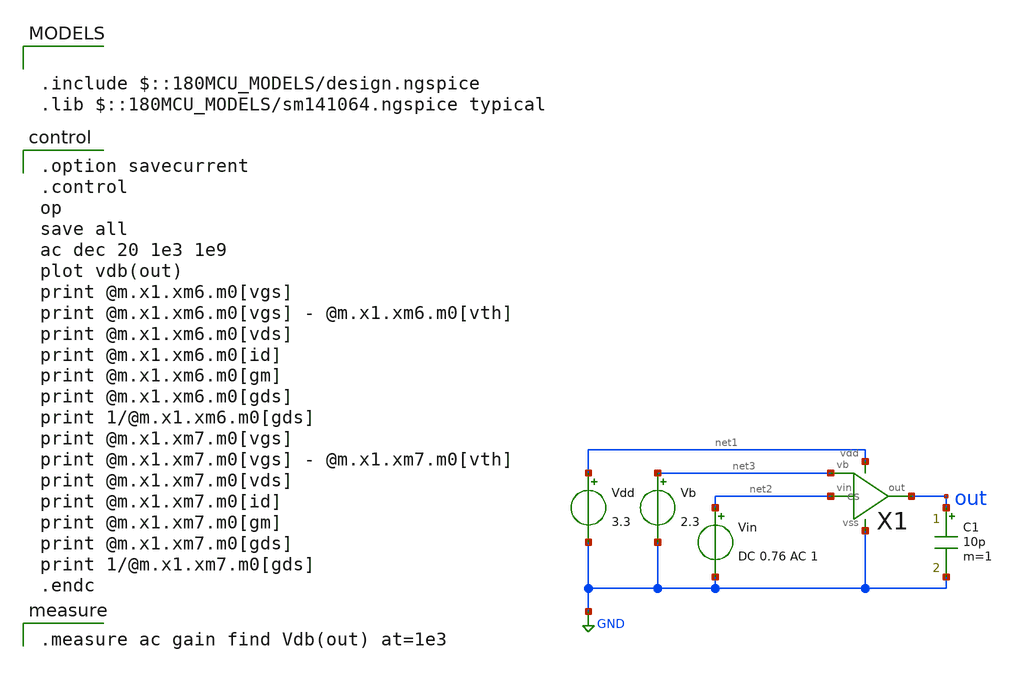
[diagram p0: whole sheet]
** sch_path: opamp/cs_ac.sch
**.subckt cs_ac
Vdd net1 GND 3.3
Vb net3 GND 2.3
Vin net2 GND DC 0.76 AC 1
X1 net2 net3 out net1 GND cs
C1 out GND 10p m=1
**** begin user architecture code

.include $::180MCU_MODELS/design.ngspice
.lib $::180MCU_MODELS/sm141064.ngspice typical


.option savecurrent
.control
op
save all
ac dec 20 1e3 1e9
plot vdb(out)
print @m.x1.xm6.m0[vgs]
print @m.x1.xm6.m0[vgs] - @m.x1.xm6.m0[vth]
print @m.x1.xm6.m0[vds]
print @m.x1.xm6.m0[id]
print @m.x1.xm6.m0[gm]
print @m.x1.xm6.m0[gds]
print 1/@m.x1.xm6.m0[gds]
print @m.x1.xm7.m0[vgs]
print @m.x1.xm7.m0[vgs] - @m.x1.xm7.m0[vth]
print @m.x1.xm7.m0[vds]
print @m.x1.xm7.m0[id]
print @m.x1.xm7.m0[gm]
print @m.x1.xm7.m0[gds]
print 1/@m.x1.xm7.m0[gds]
.endc


.measure ac gain find Vdb(out) at=1e3

**** end user architecture code
**.ends

* expanding   symbol:  cs.sym # of pins=5
** sym_path: cs.sym
** sch_path: cs.sch
.subckt cs vin vb out vdd vss
*.ipin vb
*.ipin vin
*.opin out
*.iopin vss
*.iopin vdd
XM6 out vb vdd vdd pfet_03v3 L=0.28u W=56u nf=1 ad='int((nf+1)/2) * W/nf * 0.18u' as='int((nf+2)/2) * W/nf * 0.18u'
+ pd='2*int((nf+1)/2) * (W/nf + 0.18u)' ps='2*int((nf+2)/2) * (W/nf + 0.18u)' nrd='0.18u / W' nrs='0.18u / W'
+ sa=0 sb=0 sd=0 m=1
XM7 out vin vss vss nfet_03v3 L=0.28u W=28u nf=1 ad='int((nf+1)/2) * W/nf * 0.18u' as='int((nf+2)/2) * W/nf * 0.18u'
+ pd='2*int((nf+1)/2) * (W/nf + 0.18u)' ps='2*int((nf+2)/2) * (W/nf + 0.18u)' nrd='0.18u / W' nrs='0.18u / W'
+ sa=0 sb=0 sd=0 m=1
.ends

.GLOBAL GND
.end
